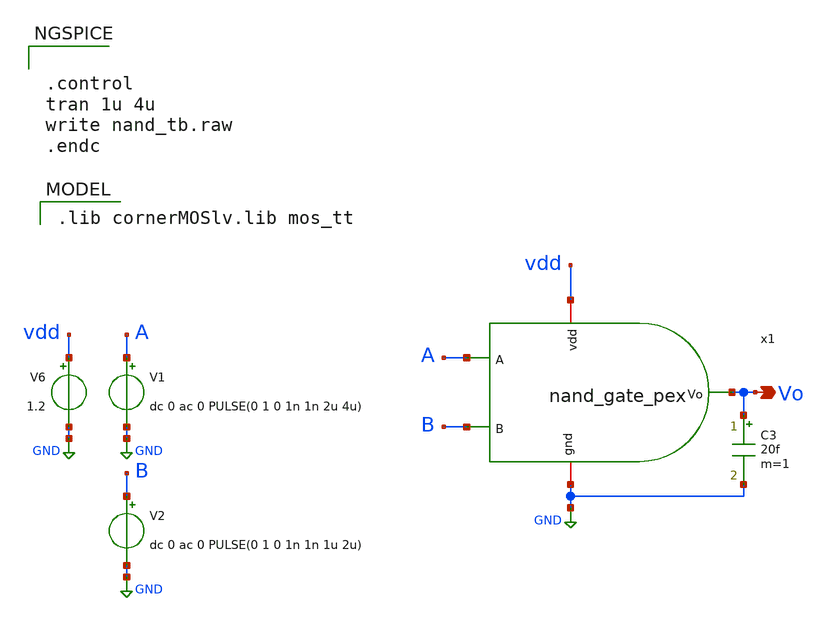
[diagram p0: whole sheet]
** sch_path: dependencies/ADC/ADC-main/schematic/xschem/nand_tb_ps.sch
**.subckt nand_tb_ps Vo
*.opin Vo
V1 A GND dc 0 ac 0 PULSE(0 1 0 1n 1n 2u 4u)
V6 vdd GND 1.2
V2 B GND dc 0 ac 0 PULSE(0 1 0 1n 1n 1u 2u)
C3 Vo GND 20f m=1
x1 vdd Vo B A GND nand_gate_pex
**** begin user architecture code


.control
tran 1u 4u
write nand_tb.raw
.endc


 .lib cornerMOSlv.lib mos_tt

**** end user architecture code
**.ends

* expanding   symbol:
*+  /home/userdata/k67D/duynk_67d/SAR_ADC_8BIT_IHP/pex/xschem_pex_symbol/nand_gate_pex.sym # of pins=5
** sym_path: dependencies/ADC/ADC-main/schematic/xschem/xschem_pex_symbol/nand_gate.sym

.subckt nand_gate_pex vdd Vo B A gnd
X0 a_n15_n246.t0 B.t0 gnd.t2 gnd.t1 sg13_lv_nmos ad=62.5f pd=0.74u as=0.1075p ps=1.34u w=0.25u
+ l=0.13u
X1 vdd.t1 A.t0 Vo.t1 vdd.t0 sg13_lv_pmos ad=0.17p pd=1.68u as=95f ps=0.88u w=0.5u l=0.13u
X2 Vo.t1 B.t0 vdd.t2 vdd.t0 sg13_lv_pmos ad=95f pd=0.88u as=0.17p ps=1.68u w=0.5u l=0.13u
X3 Vo.t0 A.t0 a_n15_n246.t0 gnd.t0 sg13_lv_nmos ad=0.1075p pd=1.34u as=62.5f ps=0.74u w=0.25u
+ l=0.13u
C0 A Vo 0.15477f
C1 B Vo 0.07214f
C2 A B 0.05121f
C3 vdd Vo 0.13452f
C4 A vdd 0.08588f
C5 B vdd 0.09489f
R0 B B.t0 15.0687
R1 gnd.n0 gnd.t1 149.24
R2 gnd.n0 gnd.t0 125.602
R3 gnd.n1 gnd.t2 17.2409
R4 gnd.n1 gnd.n0 6.88979
R5 gnd gnd.n1 0.0923197
R6 A A.t0 15.0665
R7 Vo.n0 Vo.t1 17.7224
R8 Vo.n0 Vo.t0 17.6641
R9 Vo Vo.n0 0.117375
R10 Vo.n0 Vo 0.0468158
R11 vdd.n1 vdd.t1 17.5381
R12 vdd.n0 vdd.t2 17.4749
R13 vdd.n3 vdd.n2 17.0005
R14 vdd.n2 vdd.n1 5.64075
R15 vdd.n2 vdd.t0 4.2505
R16 vdd.n1 vdd.n0 0.137308
R17 vdd vdd.n3 0.0569602
R18 vdd.n3 vdd.n0 0.0121814
C6 Vo gnd 0.12333f
C7 A gnd 0.20741f
C8 B gnd 0.23365f
C9 vdd gnd 0.17173f
.ends

.GLOBAL GND
.end
